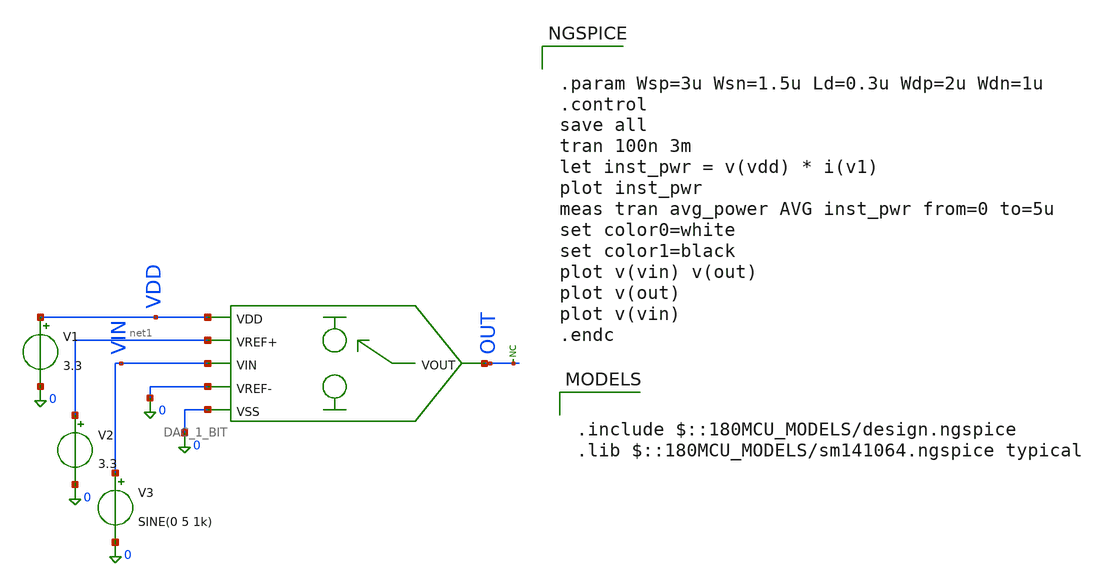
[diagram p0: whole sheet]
** sch_path: src/schematics/dac_1bit/DAC_1_BIT_TB.sch
**.subckt DAC_1_BIT_TB
V1 VDD 0 3.3
V2 net1 0 3.3
V3 VIN 0 SINE(0 5 1k)
* noconn OUT
x1 VDD net1 VIN OUT 0 0 DAC_1_BIT
**** begin user architecture code


.param Wsp=3u Wsn=1.5u Ld=0.3u Wdp=2u Wdn=1u
.control
save all
tran 100n 3m
let inst_pwr = v(vdd) * i(v1)
plot inst_pwr
meas tran avg_power AVG inst_pwr from=0 to=5u
set color0=white
set color1=black
plot v(vin) v(out)
plot v(out)
plot v(vin)
.endc




.include $::180MCU_MODELS/design.ngspice
.lib $::180MCU_MODELS/sm141064.ngspice typical

**** end user architecture code
**.ends

* expanding   symbol:  dac_1bit/DAC_1_BIT.sym # of pins=6
** sym_path: src/schematics/dac_1bit/DAC_1_BIT.sym
** sch_path: src/schematics/dac_1bit/DAC_1_BIT.sch
.subckt DAC_1_BIT VDD VREF+ VIN VOUT VREF- VSS
*.ipin VIN
*.ipin VREF+
*.ipin VREF-
*.opin VOUT
*.ipin VDD
*.ipin VSS
XM1 net1 net2 VREF+ VSS nfet_03v3 L=Ld W=Wdn nf=2 ad='int((nf+1)/2) * W/nf * 0.18u' as='int((nf+2)/2) * W/nf * 0.18u'
+ pd='2*int((nf+1)/2) * (W/nf + 0.18u)' ps='2*int((nf+2)/2) * (W/nf + 0.18u)' nrd='0.18u / W' nrs='0.18u / W'
+ sa=0 sb=0 sd=0 m=1
XM2 net1 VIN VREF+ VDD pfet_03v3 L=Ld W=Wdp nf=2 ad='int((nf+1)/2) * W/nf * 0.18u' as='int((nf+2)/2) * W/nf * 0.18u'
+ pd='2*int((nf+1)/2) * (W/nf + 0.18u)' ps='2*int((nf+2)/2) * (W/nf + 0.18u)' nrd='0.18u / W' nrs='0.18u / W'
+ sa=0 sb=0 sd=0 m=1
XM3 net1 VIN VREF- VSS nfet_03v3 L=Ld W=Wdn nf=2 ad='int((nf+1)/2) * W/nf * 0.18u' as='int((nf+2)/2) * W/nf * 0.18u'
+ pd='2*int((nf+1)/2) * (W/nf + 0.18u)' ps='2*int((nf+2)/2) * (W/nf + 0.18u)' nrd='0.18u / W' nrs='0.18u / W'
+ sa=0 sb=0 sd=0 m=1
XM4 net1 net2 VREF- VDD pfet_03v3 L=Ld W=Wdp nf=2 ad='int((nf+1)/2) * W/nf * 0.18u' as='int((nf+2)/2) * W/nf * 0.18u'
+ pd='2*int((nf+1)/2) * (W/nf + 0.18u)' ps='2*int((nf+2)/2) * (W/nf + 0.18u)' nrd='0.18u / W' nrs='0.18u / W'
+ sa=0 sb=0 sd=0 m=1
XM5 net2 VIN VDD VDD pfet_03v3 L=Ld W=Wsp nf=1 ad='int((nf+1)/2) * W/nf * 0.18u' as='int((nf+2)/2) * W/nf * 0.18u'
+ pd='2*int((nf+1)/2) * (W/nf + 0.18u)' ps='2*int((nf+2)/2) * (W/nf + 0.18u)' nrd='0.18u / W' nrs='0.18u / W'
+ sa=0 sb=0 sd=0 m=1
XM6 net2 VIN VSS VSS nfet_03v3 L=Ld W=Wsn nf=1 ad='int((nf+1)/2) * W/nf * 0.18u' as='int((nf+2)/2) * W/nf * 0.18u'
+ pd='2*int((nf+1)/2) * (W/nf + 0.18u)' ps='2*int((nf+2)/2) * (W/nf + 0.18u)' nrd='0.18u / W' nrs='0.18u / W'
+ sa=0 sb=0 sd=0 m=1
XM7 VOUT net1 VDD VDD pfet_03v3 L=Ld W=Wsp nf=1 ad='int((nf+1)/2) * W/nf * 0.18u' as='int((nf+2)/2) * W/nf * 0.18u'
+ pd='2*int((nf+1)/2) * (W/nf + 0.18u)' ps='2*int((nf+2)/2) * (W/nf + 0.18u)' nrd='0.18u / W' nrs='0.18u / W'
+ sa=0 sb=0 sd=0 m=1
XM8 VOUT net1 VSS VSS nfet_03v3 L=Ld W=Wsn nf=1 ad='int((nf+1)/2) * W/nf * 0.18u' as='int((nf+2)/2) * W/nf * 0.18u'
+ pd='2*int((nf+1)/2) * (W/nf + 0.18u)' ps='2*int((nf+2)/2) * (W/nf + 0.18u)' nrd='0.18u / W' nrs='0.18u / W'
+ sa=0 sb=0 sd=0 m=1
.ends

.end
